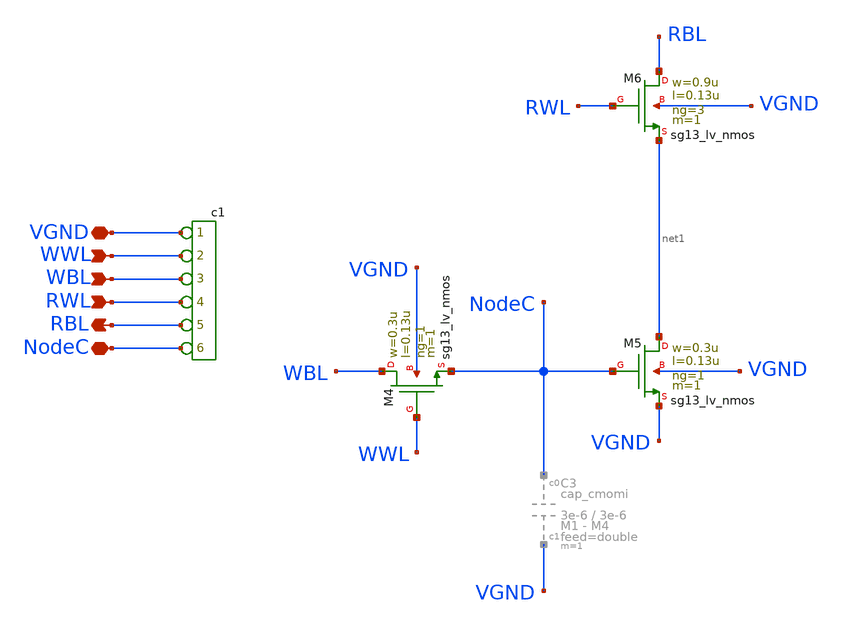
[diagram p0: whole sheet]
** sch_path: macros/heichips26_analog_project/macros/dramcell_2_0/schematic/xschem/dramcell_2_0.sch
**.subckt dramcell_2_0 RBL WWL WBL RWL VGND NodeC
*.opin RBL
*.ipin WWL
*.ipin WBL
*.ipin RWL
*.iopin VGND
*.iopin NodeC
XM4 WBL WWL NodeC VGND sg13_lv_nmos w=0.3u l=0.13u ng=1 m=1 mm_ok=1
XM5 net1 NodeC VGND VGND sg13_lv_nmos w=0.3u l=0.13u ng=1 m=1 mm_ok=1
XM6 RBL RWL net1 VGND sg13_lv_nmos w=0.9u l=0.13u ng=3 m=1 mm_ok=1
*connector(6,1) ?1 VGND ?1 WWL ?1 WBL ?1 RWL ?1 RBL ?1 NodeC
**.ends
.end
